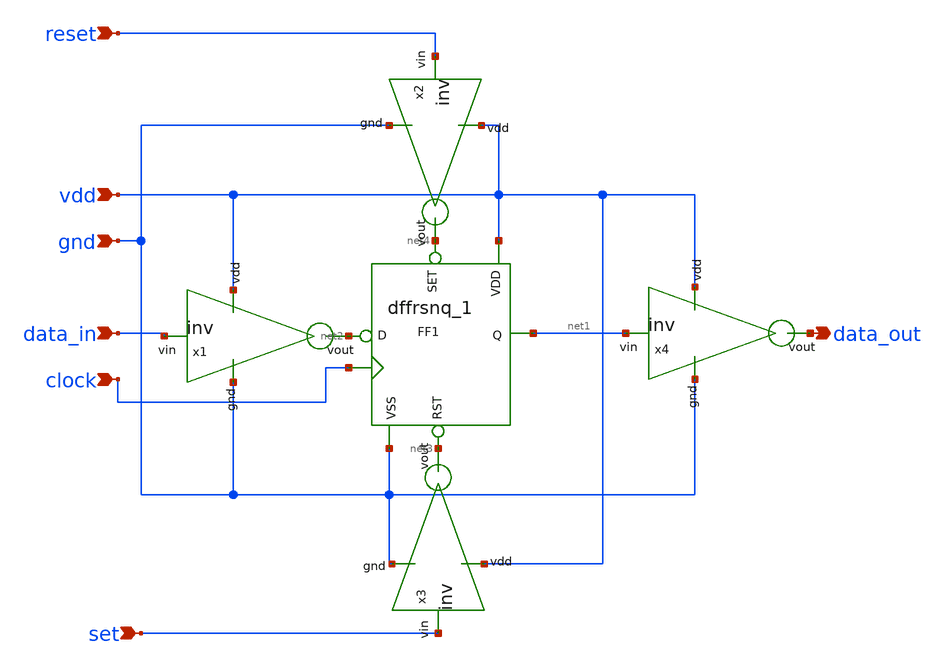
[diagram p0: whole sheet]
** sch_path: SAR_ADC/xschem/designs/ff.sch
**.subckt ff data_in clock vdd gnd data_out set reset
*.ipin data_in
*.ipin clock
*.ipin vdd
*.ipin gnd
*.opin data_out
*.ipin set
*.ipin reset
XFF1 net2 net3 net4 clock net1 vdd gnd gnd gnd gf180mcu_fd_sc_mcu7t5v0__dffrsnq_1
x1 vdd gnd net2 data_in inv cl=0.28u wp=0.44u wn=0.22u wx=0.22u
x2 vdd gnd net4 reset inv cl=0.28u wp=0.44u wn=0.22u wx=0.22u
x3 vdd gnd net3 set inv cl=0.28u wp=0.44u wn=0.22u wx=0.22u
x4 vdd gnd data_out net1 inv cl=0.28u wp=0.44u wn=0.22u wx=0.22u
**.ends

* expanding   symbol:  inv.sym # of pins=4
** sym_path: SAR_ADC/xschem/designs/inv.sym
** sch_path: SAR_ADC/xschem/designs/inv.sch
.subckt inv vdd gnd vout vin  cl=0.28u wp=0.44u wn=0.22u wx=0.22u
*.ipin gnd
*.ipin vdd
*.ipin vin
*.opin vout
XM1 gnd vin vout gnd nfet_03v3 L=0.28u W=8u nf=1 ad='int((nf+1)/2) * W/nf * 0.18u' as='int((nf+2)/2) * W/nf * 0.18u'
+ pd='2*int((nf+1)/2) * (W/nf + 0.18u)' ps='2*int((nf+2)/2) * (W/nf + 0.18u)' nrd='0.18u / W' nrs='0.18u / W'
+ sa=0 sb=0 sd=0 m=1
XM2 vdd vin vout vdd pfet_03v3 L=0.28u W=8u nf=1 ad='int((nf+1)/2) * W/nf * 0.18u' as='int((nf+2)/2) * W/nf * 0.18u'
+ pd='2*int((nf+1)/2) * (W/nf + 0.18u)' ps='2*int((nf+2)/2) * (W/nf + 0.18u)' nrd='0.18u / W' nrs='0.18u / W'
+ sa=0 sb=0 sd=0 m=1
.ends

.end
